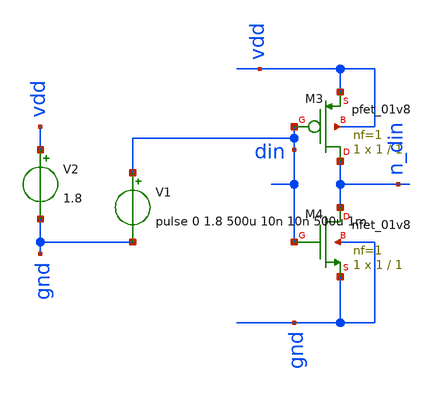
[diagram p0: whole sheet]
** sch_path: Schematics/sim_inverter.sch
**.subckt sim_inverter
XM3 n_din din vdd vdd sky130_fd_pr__pfet_01v8 L=1 W=1 nf=1 ad='int((nf+1)/2) * W/nf * 0.29' as='int((nf+2)/2) * W/nf * 0.29'
+ pd='2*int((nf+1)/2) * (W/nf + 0.29)' ps='2*int((nf+2)/2) * (W/nf + 0.29)' nrd='0.29 / W' nrs='0.29 / W'
+ sa=0 sb=0 sd=0 mult=1 m=1
XM4 n_din din gnd gnd sky130_fd_pr__nfet_01v8 L=1 W=1 nf=1 ad='int((1 + 1)/2) * 1 / 1 * 0.29' as='int((1 + 2)/2) * 1 / 1 * 0.29'
+ pd='2*int((1 + 1)/2) * (1 / 1 + 0.29)' ps='2*int((1 + 2)/2) * (1 / 1 + 0.29)' nrd='0.29 / 1 ' nrs='0.29 / 1 '
+ sa=0 sb=0 sd=0 mult=1 m=1
V1 din gnd pulse 0 1.8 500u 10n 10n 500u 1m
V2 vdd gnd 1.8
**** begin user architecture code

** opencircuitdesign pdks install
.lib $::SKYWATER_MODELS/sky130.lib.spice tt


**** end user architecture code
**.ends
**** begin user architecture code

* .option SCALE=1e-6
.option method=gear seed=12
.control
save all
tran 0.1m 1m
write sim_inverter.raw
plot din n_din
.endc


**** end user architecture code
.end
